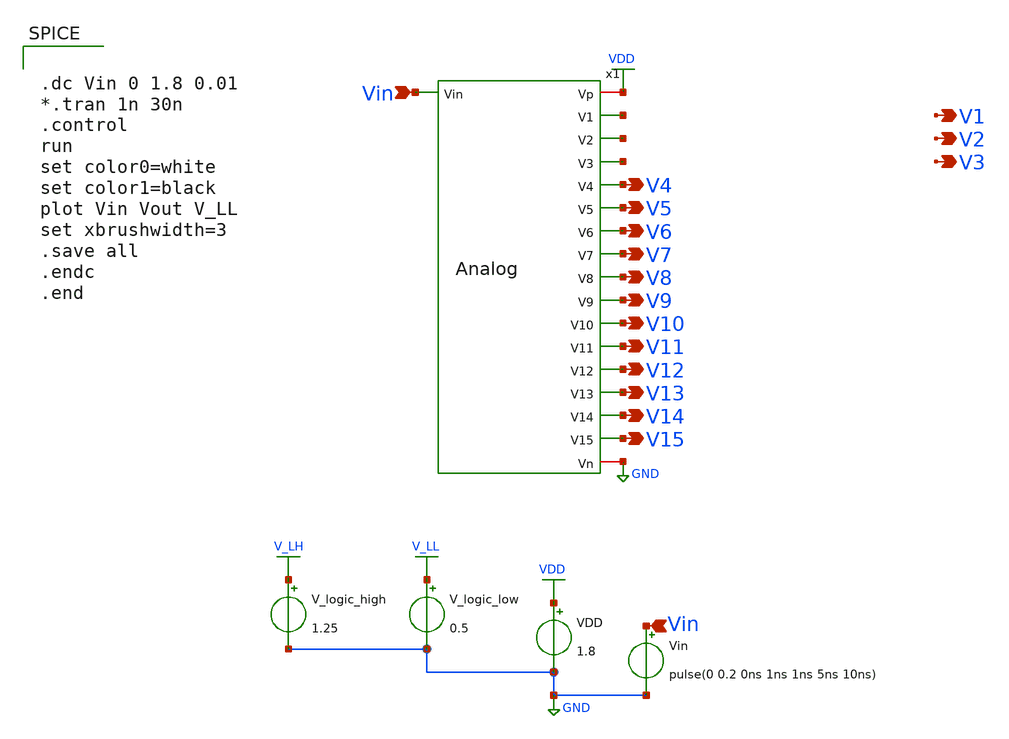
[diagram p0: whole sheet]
** sch_path: xschem/Vth_sch/Pre_layout/Analog_with_sub.sch
**.subckt Analog_with_sub Vin V1 Vin V2 V4 V5 V6 V7 V8 V9 V10 V11 V12 V13 V14 V15 V3
*.ipin Vin
*.opin V1
*.ipin Vin
*.opin V2
*.opin V4
*.opin V5
*.opin V6
*.opin V7
*.opin V8
*.opin V9
*.opin V10
*.opin V11
*.opin V12
*.opin V13
*.opin V14
*.opin V15
*.opin V3
VDD VDD GND 1.8
Vin Vin GND pulse(0 0.2 0ns 1ns 1ns 5ns 10ns)
V_logic_high V_LH GND 1.25
V_logic_low V_LL GND 0.5
x1 VDD Vin net1 net2 net3 V4 V5 V6 V7 V8 V9 V10 V11 V12 V13 V14 V15 GND Analog
**** begin user architecture code


.lib /usr/local/share/pdk/sky130A/libs.tech/ngspice/sky130.lib.spice tt

.save all





.dc Vin 0 1.8 0.01
*.tran 1n 30n
.control
run
set color0=white
set color1=black
plot Vin Vout V_LL
set xbrushwidth=3
.save all
.endc
.end


**** end user architecture code
**.ends
.GLOBAL VDD
.GLOBAL GND
.GLOBAL V_LH
.GLOBAL V_LL
.end
